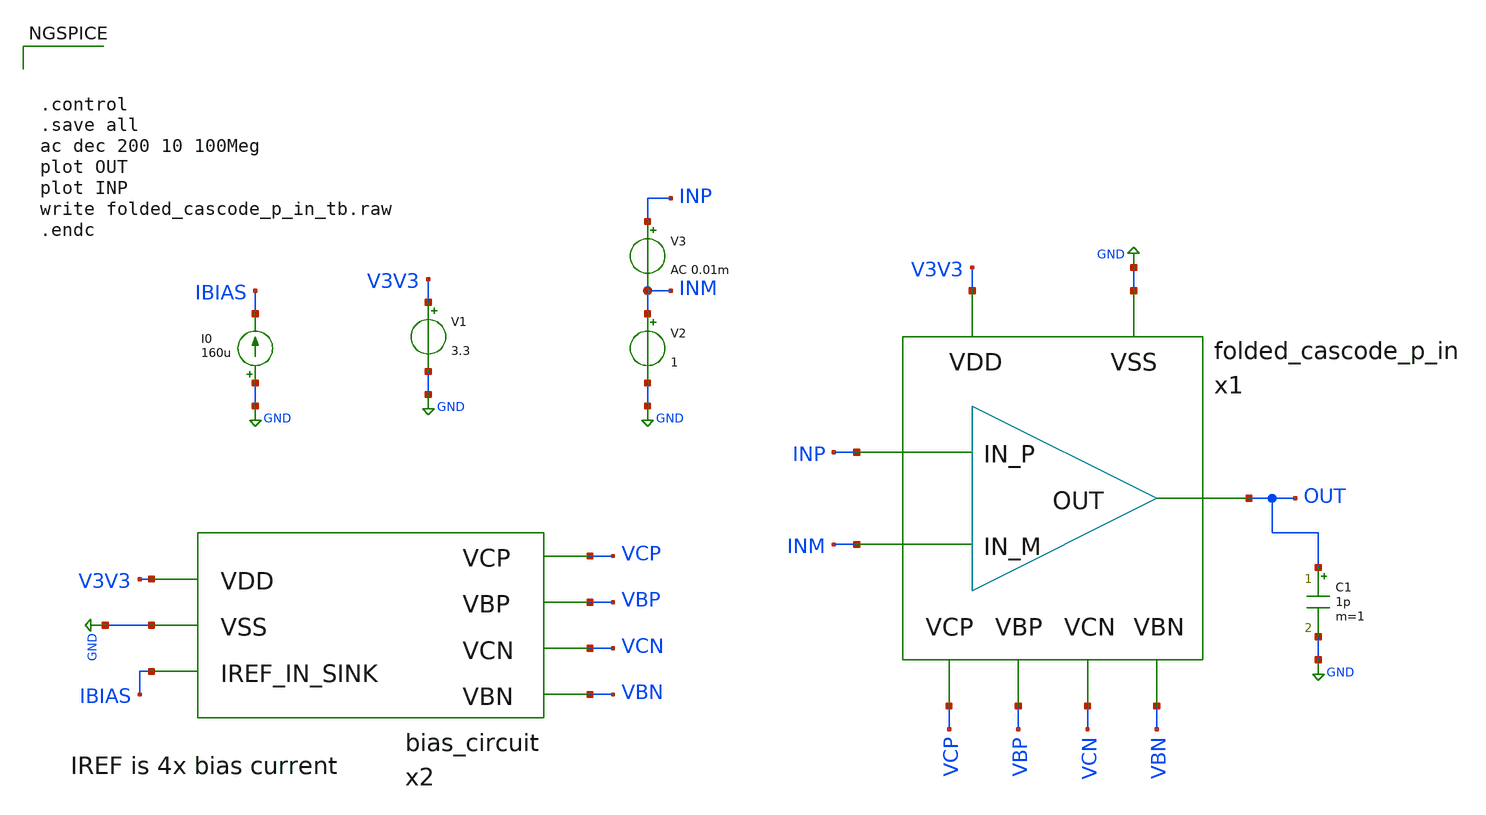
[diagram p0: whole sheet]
** sch_path: design/folded-cascode-p-in/folded_cascode_p_in_tb.sch
**.subckt folded_cascode_p_in_tb
V1 V3V3 GND 3.3
I0 GND IBIAS 160u
V2 INM GND 1
V3 INP INM AC 0.01m
C1 OUT GND 1p m=1
x2 V3V3 GND VCP VBP VCN VBN IBIAS bias_circuit
x1 INP INM OUT V3V3 GND VCP VBP VCN VBN folded_cascode_p_in
**** begin user architecture code



.control
.save all
ac dec 200 10 100Meg
plot OUT
plot INP
write folded_cascode_p_in_tb.raw
.endc



.include $::SKYWATER_MODELS/cells/nfet_01v8/sky130_fd_pr__nfet_01v8__tt.corner.spice
.include $::SKYWATER_MODELS/cells/nfet_01v8_lvt/sky130_fd_pr__nfet_01v8_lvt__tt.corner.spice
.include $::SKYWATER_MODELS/cells/pfet_01v8/sky130_fd_pr__pfet_01v8__tt.corner.spice
.include $::SKYWATER_MODELS/cells/nfet_03v3_nvt/sky130_fd_pr__nfet_03v3_nvt__tt.corner.spice
.include $::SKYWATER_MODELS/cells/nfet_05v0_nvt/sky130_fd_pr__nfet_05v0_nvt__tt.corner.spice
.include $::SKYWATER_MODELS/cells/esd_nfet_01v8/sky130_fd_pr__esd_nfet_01v8__tt.corner.spice
.include $::SKYWATER_MODELS/cells/pfet_01v8_lvt/sky130_fd_pr__pfet_01v8_lvt__tt.corner.spice
.include $::SKYWATER_MODELS/cells/pfet_01v8_hvt/sky130_fd_pr__pfet_01v8_hvt__tt.corner.spice
.include $::SKYWATER_MODELS/cells/esd_pfet_g5v0d10v5/sky130_fd_pr__esd_pfet_g5v0d10v5__tt.corner.spice
.include $::SKYWATER_MODELS/cells/pfet_g5v0d10v5/sky130_fd_pr__pfet_g5v0d10v5__tt.corner.spice
.include $::SKYWATER_MODELS/cells/pfet_g5v0d16v0/sky130_fd_pr__pfet_g5v0d16v0__tt.corner.spice
.include $::SKYWATER_MODELS/cells/nfet_g5v0d10v5/sky130_fd_pr__nfet_g5v0d10v5__tt.corner.spice
.include $::SKYWATER_MODELS/cells/nfet_g5v0d16v0/sky130_fd_pr__nfet_g5v0d16v0__tt_discrete.corner.spice
.include $::SKYWATER_MODELS/cells/esd_nfet_g5v0d10v5/sky130_fd_pr__esd_nfet_g5v0d10v5__tt.corner.spice
.include $::SKYWATER_MODELS/models/corners/tt/nonfet.spice
* Mismatch parameters
.include $::SKYWATER_MODELS/cells/nfet_01v8/sky130_fd_pr__nfet_01v8__mismatch.corner.spice
.include $::SKYWATER_MODELS/cells/pfet_01v8/sky130_fd_pr__pfet_01v8__mismatch.corner.spice
.include $::SKYWATER_MODELS/cells/nfet_01v8_lvt/sky130_fd_pr__nfet_01v8_lvt__mismatch.corner.spice
.include $::SKYWATER_MODELS/cells/pfet_01v8_lvt/sky130_fd_pr__pfet_01v8_lvt__mismatch.corner.spice
.include $::SKYWATER_MODELS/cells/pfet_01v8_hvt/sky130_fd_pr__pfet_01v8_hvt__mismatch.corner.spice
.include $::SKYWATER_MODELS/cells/nfet_g5v0d10v5/sky130_fd_pr__nfet_g5v0d10v5__mismatch.corner.spice
.include $::SKYWATER_MODELS/cells/pfet_g5v0d10v5/sky130_fd_pr__pfet_g5v0d10v5__mismatch.corner.spice
.include $::SKYWATER_MODELS/cells/nfet_05v0_nvt/sky130_fd_pr__nfet_05v0_nvt__mismatch.corner.spice
.include $::SKYWATER_MODELS/cells/nfet_03v3_nvt/sky130_fd_pr__nfet_03v3_nvt__mismatch.corner.spice
* Resistor$::SKYWATER_MODELS/Capacitor
.include $::SKYWATER_MODELS/models/r+c/res_typical__cap_typical.spice
.include $::SKYWATER_MODELS/models/r+c/res_typical__cap_typical__lin.spice
* Special cells
.include $::SKYWATER_MODELS/models/corners/tt/specialized_cells.spice
* All models
.include $::SKYWATER_MODELS/models/all.spice
* Corner
.include $::SKYWATER_MODELS/models/corners/tt/rf.spice

**** end user architecture code
**.ends

* expanding   symbol:  /home/wbraun/projects/open-pmic/design/bias-circuit/bias_circuit.sym # of
*+ pins=7
** sym_path: design/bias-circuit/bias_circuit.sym
** sch_path: design/bias-circuit/bias_circuit.sch
.subckt bias_circuit VDD VSS VCP VBP VCN VBN IREF_IN_SINK
*.ipin IREF_IN_SINK
*.ipin VCN
*.ipin VSS
*.ipin VDD
*.ipin VCP
*.ipin VBP
*.ipin VBN
XM2 VBP VBP VDD VDD sky130_fd_pr__pfet_g5v0d10v5 L=1 W=12 nf=1 ad='int((nf+1)/2) * W/nf * 0.29' as='int((nf+2)/2) * W/nf * 0.29'
+ pd='2*int((nf+1)/2) * (W/nf + 0.29)' ps='2*int((nf+2)/2) * (W/nf + 0.29)' nrd='0.29 / W' nrs='0.29 / W'
+ sa=0 sb=0 sd=0 mult=1 m=1
XM3 net1 VBP VDD VDD sky130_fd_pr__pfet_g5v0d10v5 L=5 W=12 nf=1 ad='int((nf+1)/2) * W/nf * 0.29' as='int((nf+2)/2) * W/nf * 0.29'
+ pd='2*int((nf+1)/2) * (W/nf + 0.29)' ps='2*int((nf+2)/2) * (W/nf + 0.29)' nrd='0.29 / W' nrs='0.29 / W'
+ sa=0 sb=0 sd=0 mult=1 m=1
XM4 VCN VBP VDD VDD sky130_fd_pr__pfet_g5v0d10v5 L=1 W=12 nf=1 ad='int((nf+1)/2) * W/nf * 0.29' as='int((nf+2)/2) * W/nf * 0.29'
+ pd='2*int((nf+1)/2) * (W/nf + 0.29)' ps='2*int((nf+2)/2) * (W/nf + 0.29)' nrd='0.29 / W' nrs='0.29 / W'
+ sa=0 sb=0 sd=0 mult=1 m=1
XM5 net1 net1 net2 VSS sky130_fd_pr__nfet_g5v0d10v5 L=1 W=12 nf=1 ad='int((nf+1)/2) * W/nf * 0.29' as='int((nf+2)/2) * W/nf * 0.29'
+ pd='2*int((nf+1)/2) * (W/nf + 0.29)' ps='2*int((nf+2)/2) * (W/nf + 0.29)' nrd='0.29 / W' nrs='0.29 / W'
+ sa=0 sb=0 sd=0 mult=4 m=4
XM6 net2 net1 VSS VSS sky130_fd_pr__nfet_g5v0d10v5 L=1 W=12 nf=1 ad='int((nf+1)/2) * W/nf * 0.29' as='int((nf+2)/2) * W/nf * 0.29'
+ pd='2*int((nf+1)/2) * (W/nf + 0.29)' ps='2*int((nf+2)/2) * (W/nf + 0.29)' nrd='0.29 / W' nrs='0.29 / W'
+ sa=0 sb=0 sd=0 mult=1 m=1
XM7 VCN VCN net2 VSS sky130_fd_pr__nfet_g5v0d10v5 L=1 W=12 nf=1 ad='int((nf+1)/2) * W/nf * 0.29' as='int((nf+2)/2) * W/nf * 0.29'
+ pd='2*int((nf+1)/2) * (W/nf + 0.29)' ps='2*int((nf+2)/2) * (W/nf + 0.29)' nrd='0.29 / W' nrs='0.29 / W'
+ sa=0 sb=0 sd=0 mult=1 m=1
XM8 VBN VBN VSS VSS sky130_fd_pr__nfet_g5v0d10v5 L=1 W=12 nf=1 ad='int((nf+1)/2) * W/nf * 0.29' as='int((nf+2)/2) * W/nf * 0.29'
+ pd='2*int((nf+1)/2) * (W/nf + 0.29)' ps='2*int((nf+2)/2) * (W/nf + 0.29)' nrd='0.29 / W' nrs='0.29 / W'
+ sa=0 sb=0 sd=0 mult=1 m=1
XM9 VBN VBP VDD VDD sky130_fd_pr__pfet_g5v0d10v5 L=1 W=12 nf=1 ad='int((nf+1)/2) * W/nf * 0.29' as='int((nf+2)/2) * W/nf * 0.29'
+ pd='2*int((nf+1)/2) * (W/nf + 0.29)' ps='2*int((nf+2)/2) * (W/nf + 0.29)' nrd='0.29 / W' nrs='0.29 / W'
+ sa=0 sb=0 sd=0 mult=1 m=1
XM10 net3 VBN VSS VSS sky130_fd_pr__nfet_g5v0d10v5 L=5 W=12 nf=1 ad='int((nf+1)/2) * W/nf * 0.29' as='int((nf+2)/2) * W/nf * 0.29'
+ pd='2*int((nf+1)/2) * (W/nf + 0.29)' ps='2*int((nf+2)/2) * (W/nf + 0.29)' nrd='0.29 / W' nrs='0.29 / W'
+ sa=0 sb=0 sd=0 mult=1 m=1
XM11 VCP VBN VSS VSS sky130_fd_pr__nfet_g5v0d10v5 L=1 W=12 nf=1 ad='int((nf+1)/2) * W/nf * 0.29' as='int((nf+2)/2) * W/nf * 0.29'
+ pd='2*int((nf+1)/2) * (W/nf + 0.29)' ps='2*int((nf+2)/2) * (W/nf + 0.29)' nrd='0.29 / W' nrs='0.29 / W'
+ sa=0 sb=0 sd=0 mult=1 m=1
XM12 net3 net3 net4 VDD sky130_fd_pr__pfet_g5v0d10v5 L=1 W=12 nf=1 ad='int((nf+1)/2) * W/nf * 0.29' as='int((nf+2)/2) * W/nf * 0.29'
+ pd='2*int((nf+1)/2) * (W/nf + 0.29)' ps='2*int((nf+2)/2) * (W/nf + 0.29)' nrd='0.29 / W' nrs='0.29 / W'
+ sa=0 sb=0 sd=0 mult=4 m=4
XM13 VCP VCP net4 VDD sky130_fd_pr__pfet_g5v0d10v5 L=1 W=12 nf=1 ad='int((nf+1)/2) * W/nf * 0.29' as='int((nf+2)/2) * W/nf * 0.29'
+ pd='2*int((nf+1)/2) * (W/nf + 0.29)' ps='2*int((nf+2)/2) * (W/nf + 0.29)' nrd='0.29 / W' nrs='0.29 / W'
+ sa=0 sb=0 sd=0 mult=1 m=1
XM14 net4 net3 VDD VDD sky130_fd_pr__pfet_g5v0d10v5 L=1 W=12 nf=1 ad='int((nf+1)/2) * W/nf * 0.29' as='int((nf+2)/2) * W/nf * 0.29'
+ pd='2*int((nf+1)/2) * (W/nf + 0.29)' ps='2*int((nf+2)/2) * (W/nf + 0.29)' nrd='0.29 / W' nrs='0.29 / W'
+ sa=0 sb=0 sd=0 mult=1 m=1
XM1 VBP IREF_IN_SINK VSS VSS sky130_fd_pr__nfet_g5v0d10v5 L=1 W=12 nf=1 ad='int((nf+1)/2) * W/nf * 0.29'
+ as='int((nf+2)/2) * W/nf * 0.29' pd='2*int((nf+1)/2) * (W/nf + 0.29)' ps='2*int((nf+2)/2) * (W/nf + 0.29)'
+ nrd='0.29 / W' nrs='0.29 / W' sa=0 sb=0 sd=0 mult=1 m=1
XM15 IREF_IN_SINK IREF_IN_SINK VSS VSS sky130_fd_pr__nfet_g5v0d10v5 L=1 W=12 nf=1 ad='int((nf+1)/2) * W/nf * 0.29'
+ as='int((nf+2)/2) * W/nf * 0.29' pd='2*int((nf+1)/2) * (W/nf + 0.29)' ps='2*int((nf+2)/2) * (W/nf + 0.29)'
+ nrd='0.29 / W' nrs='0.29 / W' sa=0 sb=0 sd=0 mult=4 m=4
.ends


* expanding   symbol:
*+  /home/wbraun/projects/open-pmic/design/folded-cascode-p-in/folded_cascode_p_in.sym # of pins=9
** sym_path: design/folded-cascode-p-in/folded_cascode_p_in.sym
** sch_path: design/folded-cascode-p-in/folded_cascode_p_in.sch
.subckt folded_cascode_p_in IN_P IN_M OUT VDD VSS VCP VBP VCN VBN
*.ipin IN_P
*.ipin IN_M
*.ipin OUT
*.ipin VDD
*.ipin VSS
*.ipin VCP
*.ipin VBP
*.ipin VCN
*.ipin VBN
XM7 net4 VBP VDD VDD sky130_fd_pr__pfet_g5v0d10v5 L=1 W=12 nf=1 ad='int((nf+1)/2) * W/nf * 0.29' as='int((nf+2)/2) * W/nf * 0.29'
+ pd='2*int((nf+1)/2) * (W/nf + 0.29)' ps='2*int((nf+2)/2) * (W/nf + 0.29)' nrd='0.29 / W' nrs='0.29 / W'
+ sa=0 sb=0 sd=0 mult=4 m=4
XM8 VS1_P IN_M net4 VDD sky130_fd_pr__pfet_g5v0d10v5 L=1 W=12 nf=1 ad='int((nf+1)/2) * W/nf * 0.29' as='int((nf+2)/2) * W/nf * 0.29'
+ pd='2*int((nf+1)/2) * (W/nf + 0.29)' ps='2*int((nf+2)/2) * (W/nf + 0.29)' nrd='0.29 / W' nrs='0.29 / W'
+ sa=0 sb=0 sd=0 mult=10 m=10
XM15 VS1_M IN_P net4 VDD sky130_fd_pr__pfet_g5v0d10v5 L=1 W=12 nf=1 ad='int((nf+1)/2) * W/nf * 0.29'
+ as='int((nf+2)/2) * W/nf * 0.29' pd='2*int((nf+1)/2) * (W/nf + 0.29)' ps='2*int((nf+2)/2) * (W/nf + 0.29)'
+ nrd='0.29 / W' nrs='0.29 / W' sa=0 sb=0 sd=0 mult=10 m=10
XM16 VS1_P VBN_INT VSS VSS sky130_fd_pr__nfet_g5v0d10v5 L=1 W=12 nf=1 ad='int((nf+1)/2) * W/nf * 0.29'
+ as='int((nf+2)/2) * W/nf * 0.29' pd='2*int((nf+1)/2) * (W/nf + 0.29)' ps='2*int((nf+2)/2) * (W/nf + 0.29)'
+ nrd='0.29 / W' nrs='0.29 / W' sa=0 sb=0 sd=0 mult=3 m=3
XM20 VS1_M VBN_INT VSS VSS sky130_fd_pr__nfet_g5v0d10v5 L=1 W=12 nf=1 ad='int((nf+1)/2) * W/nf * 0.29'
+ as='int((nf+2)/2) * W/nf * 0.29' pd='2*int((nf+1)/2) * (W/nf + 0.29)' ps='2*int((nf+2)/2) * (W/nf + 0.29)'
+ nrd='0.29 / W' nrs='0.29 / W' sa=0 sb=0 sd=0 mult=3 m=3
XM22 net3 VCP net1 VDD sky130_fd_pr__pfet_g5v0d10v5 L=1 W=12 nf=1 ad='int((nf+1)/2) * W/nf * 0.29' as='int((nf+2)/2) * W/nf * 0.29'
+ pd='2*int((nf+1)/2) * (W/nf + 0.29)' ps='2*int((nf+2)/2) * (W/nf + 0.29)' nrd='0.29 / W' nrs='0.29 / W'
+ sa=0 sb=0 sd=0 mult=1 m=1
XM23 net1 net3 VDD VDD sky130_fd_pr__pfet_g5v0d10v5 L=1 W=12 nf=1 ad='int((nf+1)/2) * W/nf * 0.29' as='int((nf+2)/2) * W/nf * 0.29'
+ pd='2*int((nf+1)/2) * (W/nf + 0.29)' ps='2*int((nf+2)/2) * (W/nf + 0.29)' nrd='0.29 / W' nrs='0.29 / W'
+ sa=0 sb=0 sd=0 mult=1 m=1
XM24 OUT VCP net2 VDD sky130_fd_pr__pfet_g5v0d10v5 L=1 W=12 nf=1 ad='int((nf+1)/2) * W/nf * 0.29' as='int((nf+2)/2) * W/nf * 0.29'
+ pd='2*int((nf+1)/2) * (W/nf + 0.29)' ps='2*int((nf+2)/2) * (W/nf + 0.29)' nrd='0.29 / W' nrs='0.29 / W'
+ sa=0 sb=0 sd=0 mult=1 m=1
XM25 net2 net3 VDD VDD sky130_fd_pr__pfet_g5v0d10v5 L=1 W=12 nf=1 ad='int((nf+1)/2) * W/nf * 0.29' as='int((nf+2)/2) * W/nf * 0.29'
+ pd='2*int((nf+1)/2) * (W/nf + 0.29)' ps='2*int((nf+2)/2) * (W/nf + 0.29)' nrd='0.29 / W' nrs='0.29 / W'
+ sa=0 sb=0 sd=0 mult=1 m=1
XM26 OUT VCN VS1_P VSS sky130_fd_pr__nfet_g5v0d10v5 L=1 W=12 nf=1 ad='int((nf+1)/2) * W/nf * 0.29' as='int((nf+2)/2) * W/nf * 0.29'
+ pd='2*int((nf+1)/2) * (W/nf + 0.29)' ps='2*int((nf+2)/2) * (W/nf + 0.29)' nrd='0.29 / W' nrs='0.29 / W'
+ sa=0 sb=0 sd=0 mult=1 m=1
XM27 net3 VCN VS1_M VSS sky130_fd_pr__nfet_g5v0d10v5 L=1 W=12 nf=1 ad='int((nf+1)/2) * W/nf * 0.29' as='int((nf+2)/2) * W/nf * 0.29'
+ pd='2*int((nf+1)/2) * (W/nf + 0.29)' ps='2*int((nf+2)/2) * (W/nf + 0.29)' nrd='0.29 / W' nrs='0.29 / W'
+ sa=0 sb=0 sd=0 mult=1 m=1
XM29 VBN_INT VBN_INT VSS VSS sky130_fd_pr__nfet_g5v0d10v5 L=1 W=12 nf=1 ad='int((nf+1)/2) * W/nf * 0.29'
+ as='int((nf+2)/2) * W/nf * 0.29' pd='2*int((nf+1)/2) * (W/nf + 0.29)' ps='2*int((nf+2)/2) * (W/nf + 0.29)'
+ nrd='0.29 / W' nrs='0.29 / W' sa=0 sb=0 sd=0 mult=1 m=1
XM30 VBN_INT VBP VDD VDD sky130_fd_pr__pfet_g5v0d10v5 L=1 W=12 nf=1 ad='int((nf+1)/2) * W/nf * 0.29'
+ as='int((nf+2)/2) * W/nf * 0.29' pd='2*int((nf+1)/2) * (W/nf + 0.29)' ps='2*int((nf+2)/2) * (W/nf + 0.29)'
+ nrd='0.29 / W' nrs='0.29 / W' sa=0 sb=0 sd=0 mult=1 m=1
.ends

.GLOBAL GND
**** begin user architecture code
[sky130_models]
**** end user architecture code
.end
